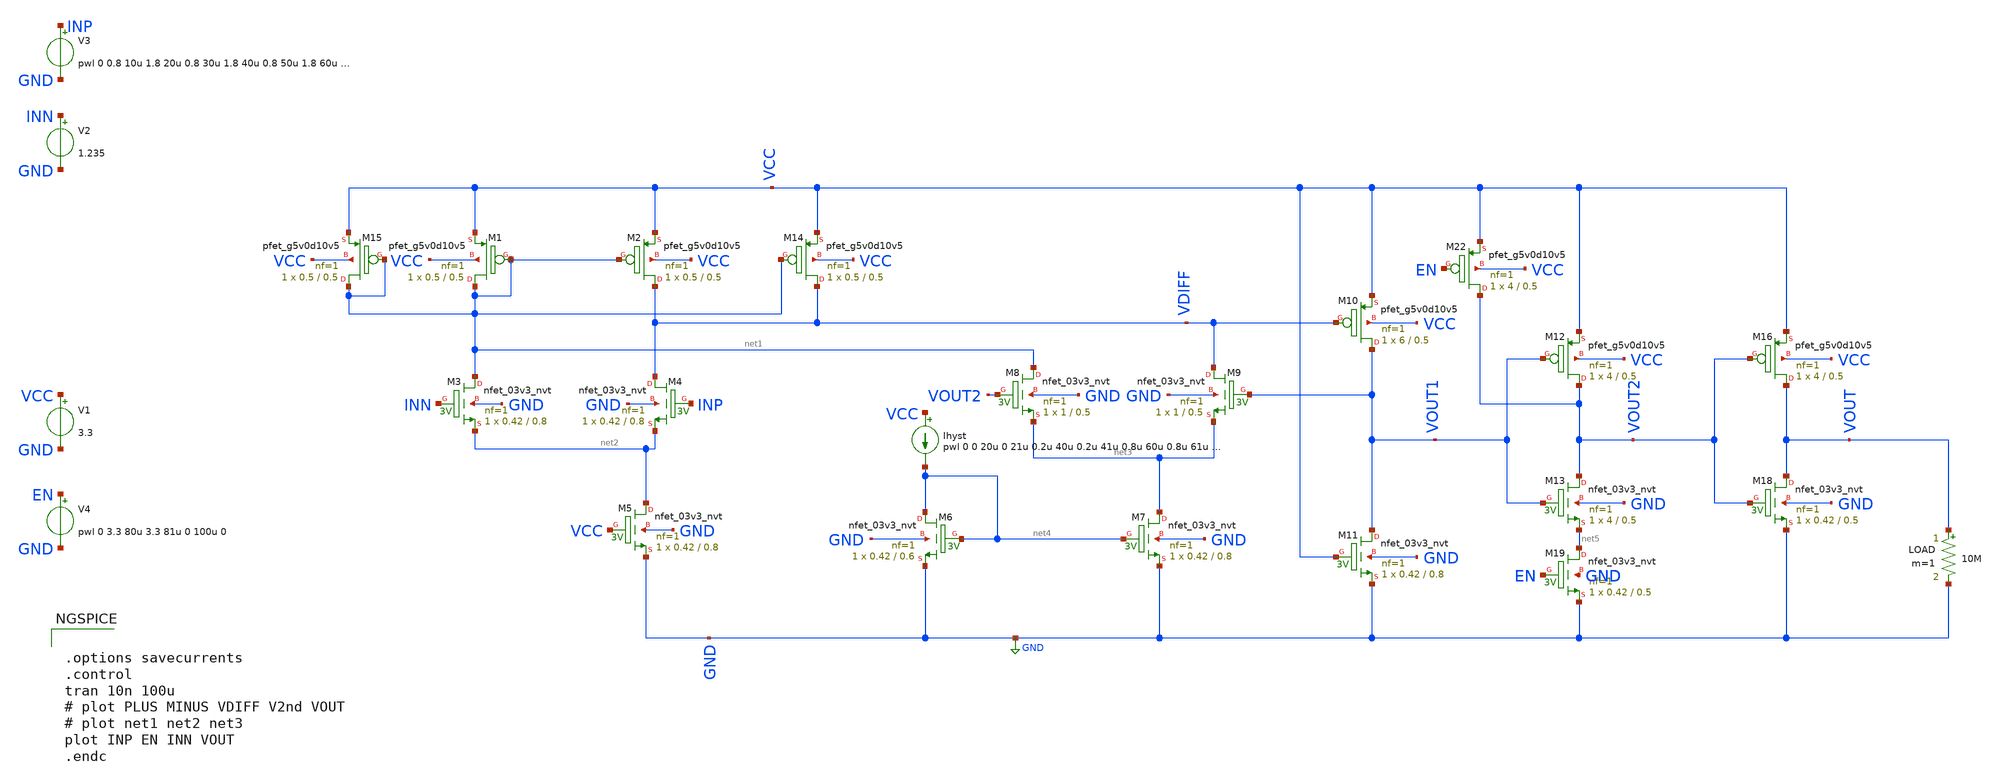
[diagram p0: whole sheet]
** sch_path: PreLayout/archive/comparator.sch
* Copyright 2020 Stefan Frederik Schippers
* Licensed under the Apache License, Version 2.0 (the "License");
* you may not use this file except in compliance with the License.
* You may obtain a copy of the License at
* https://www.apache.org/licenses/LICENSE-2.0
* Unless required by applicable law or agreed to in writing, software
* distributed under the License is distributed on an "AS IS" BASIS,
* WITHOUT WARRANTIES OR CONDITIONS OF ANY KIND, either express or implied.
* See the License for the specific language governing permissions and
* limitations under the License.
**.subckt comparator
Ihyst VCC net4 pwl 0 0 20u 0 21u 0.2u 40u 0.2u 41u 0.8u 60u 0.8u 61u 10u 100u 10u
V1 VCC GND 3.3
V2 INN GND 1.235
V3 INP GND pwl 0 0.8 10u 1.8 20u 0.8 30u 1.8 40u 0.8 50u 1.8 60u 0.8 70u 1.8 80u 0.8 90u 1.8 100u
+ 0.8
XM3 net1 INN net2 GND sky130_fd_pr__nfet_03v3_nvt L=0.8 W=0.42 nf=1 ad='int((nf+1)/2) * W/nf * 0.29'
+ as='int((nf+2)/2) * W/nf * 0.29' pd='2*int((nf+1)/2) * (W/nf + 0.29)' ps='2*int((nf+2)/2) * (W/nf + 0.29)'
+ nrd='0.29 / W' nrs='0.29 / W' sa=0 sb=0 sd=0 mult=1 m=1
XM4 VDIFF INP net2 GND sky130_fd_pr__nfet_03v3_nvt L=0.8 W=0.42 nf=1 ad='int((nf+1)/2) * W/nf * 0.29'
+ as='int((nf+2)/2) * W/nf * 0.29' pd='2*int((nf+1)/2) * (W/nf + 0.29)' ps='2*int((nf+2)/2) * (W/nf + 0.29)'
+ nrd='0.29 / W' nrs='0.29 / W' sa=0 sb=0 sd=0 mult=1 m=1
XM8 net1 VOUT2 net3 GND sky130_fd_pr__nfet_03v3_nvt L=0.5 W=1 nf=1 ad='int((nf+1)/2) * W/nf * 0.29' as='int((nf+2)/2) * W/nf * 0.29'
+ pd='2*int((nf+1)/2) * (W/nf + 0.29)' ps='2*int((nf+2)/2) * (W/nf + 0.29)' nrd='0.29 / W' nrs='0.29 / W'
+ sa=0 sb=0 sd=0 mult=1 m=1
XM9 VDIFF VOUT1 net3 GND sky130_fd_pr__nfet_03v3_nvt L=0.5 W=1 nf=1 ad='int((nf+1)/2) * W/nf * 0.29'
+ as='int((nf+2)/2) * W/nf * 0.29' pd='2*int((nf+1)/2) * (W/nf + 0.29)' ps='2*int((nf+2)/2) * (W/nf + 0.29)'
+ nrd='0.29 / W' nrs='0.29 / W' sa=0 sb=0 sd=0 mult=1 m=1
XM5 net2 VCC GND GND sky130_fd_pr__nfet_03v3_nvt L=0.8 W=0.42 nf=1 ad='int((nf+1)/2) * W/nf * 0.29' as='int((nf+2)/2) * W/nf * 0.29'
+ pd='2*int((nf+1)/2) * (W/nf + 0.29)' ps='2*int((nf+2)/2) * (W/nf + 0.29)' nrd='0.29 / W' nrs='0.29 / W'
+ sa=0 sb=0 sd=0 mult=1 m=1
XM2 VDIFF net1 VCC VCC sky130_fd_pr__pfet_g5v0d10v5 L=0.5 W=0.5 nf=1 ad='int((nf+1)/2) * W/nf * 0.29'
+ as='int((nf+2)/2) * W/nf * 0.29' pd='2*int((nf+1)/2) * (W/nf + 0.29)' ps='2*int((nf+2)/2) * (W/nf + 0.29)'
+ nrd='0.29 / W' nrs='0.29 / W' sa=0 sb=0 sd=0 mult=1 m=1
XM1 net1 net1 VCC VCC sky130_fd_pr__pfet_g5v0d10v5 L=0.5 W=0.5 nf=1 ad='int((nf+1)/2) * W/nf * 0.29'
+ as='int((nf+2)/2) * W/nf * 0.29' pd='2*int((nf+1)/2) * (W/nf + 0.29)' ps='2*int((nf+2)/2) * (W/nf + 0.29)'
+ nrd='0.29 / W' nrs='0.29 / W' sa=0 sb=0 sd=0 mult=1 m=1
XM12 VOUT2 VOUT1 VCC VCC sky130_fd_pr__pfet_g5v0d10v5 L=0.5 W=4 nf=1 ad='int((nf+1)/2) * W/nf * 0.29'
+ as='int((nf+2)/2) * W/nf * 0.29' pd='2*int((nf+1)/2) * (W/nf + 0.29)' ps='2*int((nf+2)/2) * (W/nf + 0.29)'
+ nrd='0.29 / W' nrs='0.29 / W' sa=0 sb=0 sd=0 mult=1 m=1
XM10 VOUT1 VDIFF VCC VCC sky130_fd_pr__pfet_g5v0d10v5 L=0.5 W=6 nf=1 ad='int((nf+1)/2) * W/nf * 0.29'
+ as='int((nf+2)/2) * W/nf * 0.29' pd='2*int((nf+1)/2) * (W/nf + 0.29)' ps='2*int((nf+2)/2) * (W/nf + 0.29)'
+ nrd='0.29 / W' nrs='0.29 / W' sa=0 sb=0 sd=0 mult=1 m=1
XM13 VOUT2 VOUT1 net5 GND sky130_fd_pr__nfet_03v3_nvt L=0.5 W=4 nf=1 ad='int((nf+1)/2) * W/nf * 0.29'
+ as='int((nf+2)/2) * W/nf * 0.29' pd='2*int((nf+1)/2) * (W/nf + 0.29)' ps='2*int((nf+2)/2) * (W/nf + 0.29)'
+ nrd='0.29 / W' nrs='0.29 / W' sa=0 sb=0 sd=0 mult=1 m=1
XM11 VOUT1 VCC GND GND sky130_fd_pr__nfet_03v3_nvt L=0.8 W=0.42 nf=1 ad='int((nf+1)/2) * W/nf * 0.29'
+ as='int((nf+2)/2) * W/nf * 0.29' pd='2*int((nf+1)/2) * (W/nf + 0.29)' ps='2*int((nf+2)/2) * (W/nf + 0.29)'
+ nrd='0.29 / W' nrs='0.29 / W' sa=0 sb=0 sd=0 mult=1 m=1
XM7 net3 net4 GND GND sky130_fd_pr__nfet_03v3_nvt L=0.8 W=0.42 nf=1 ad='int((nf+1)/2) * W/nf * 0.29'
+ as='int((nf+2)/2) * W/nf * 0.29' pd='2*int((nf+1)/2) * (W/nf + 0.29)' ps='2*int((nf+2)/2) * (W/nf + 0.29)'
+ nrd='0.29 / W' nrs='0.29 / W' sa=0 sb=0 sd=0 mult=1 m=1
XM6 net4 net4 GND GND sky130_fd_pr__nfet_03v3_nvt L=0.6 W=0.42 nf=1 ad='int((nf+1)/2) * W/nf * 0.29'
+ as='int((nf+2)/2) * W/nf * 0.29' pd='2*int((nf+1)/2) * (W/nf + 0.29)' ps='2*int((nf+2)/2) * (W/nf + 0.29)'
+ nrd='0.29 / W' nrs='0.29 / W' sa=0 sb=0 sd=0 mult=1 m=1
V4 EN GND pwl 0 3.3 80u 3.3 81u 0 100u 0
LOAD VOUT GND 10M m=1
XM14 VDIFF net1 VCC VCC sky130_fd_pr__pfet_g5v0d10v5 L=0.5 W=0.5 nf=1 ad='int((nf+1)/2) * W/nf * 0.29'
+ as='int((nf+2)/2) * W/nf * 0.29' pd='2*int((nf+1)/2) * (W/nf + 0.29)' ps='2*int((nf+2)/2) * (W/nf + 0.29)'
+ nrd='0.29 / W' nrs='0.29 / W' sa=0 sb=0 sd=0 mult=1 m=1
XM15 net1 net1 VCC VCC sky130_fd_pr__pfet_g5v0d10v5 L=0.5 W=0.5 nf=1 ad='int((nf+1)/2) * W/nf * 0.29'
+ as='int((nf+2)/2) * W/nf * 0.29' pd='2*int((nf+1)/2) * (W/nf + 0.29)' ps='2*int((nf+2)/2) * (W/nf + 0.29)'
+ nrd='0.29 / W' nrs='0.29 / W' sa=0 sb=0 sd=0 mult=1 m=1
XM16 VOUT VOUT2 VCC VCC sky130_fd_pr__pfet_g5v0d10v5 L=0.5 W=4 nf=1 ad='int((nf+1)/2) * W/nf * 0.29'
+ as='int((nf+2)/2) * W/nf * 0.29' pd='2*int((nf+1)/2) * (W/nf + 0.29)' ps='2*int((nf+2)/2) * (W/nf + 0.29)'
+ nrd='0.29 / W' nrs='0.29 / W' sa=0 sb=0 sd=0 mult=1 m=1
XM18 VOUT VOUT2 GND GND sky130_fd_pr__nfet_03v3_nvt L=0.5 W=0.42 nf=1 ad='int((nf+1)/2) * W/nf * 0.29'
+ as='int((nf+2)/2) * W/nf * 0.29' pd='2*int((nf+1)/2) * (W/nf + 0.29)' ps='2*int((nf+2)/2) * (W/nf + 0.29)'
+ nrd='0.29 / W' nrs='0.29 / W' sa=0 sb=0 sd=0 mult=1 m=1
XM19 net5 EN GND GND sky130_fd_pr__nfet_03v3_nvt L=0.5 W=0.42 nf=1 ad='int((nf+1)/2) * W/nf * 0.29' as='int((nf+2)/2) * W/nf * 0.29'
+ pd='2*int((nf+1)/2) * (W/nf + 0.29)' ps='2*int((nf+2)/2) * (W/nf + 0.29)' nrd='0.29 / W' nrs='0.29 / W'
+ sa=0 sb=0 sd=0 mult=1 m=1
XM22 VOUT2 EN VCC VCC sky130_fd_pr__pfet_g5v0d10v5 L=0.5 W=4 nf=1 ad='int((nf+1)/2) * W/nf * 0.29' as='int((nf+2)/2) * W/nf * 0.29'
+ pd='2*int((nf+1)/2) * (W/nf + 0.29)' ps='2*int((nf+2)/2) * (W/nf + 0.29)' nrd='0.29 / W' nrs='0.29 / W'
+ sa=0 sb=0 sd=0 mult=1 m=1
**** begin user architecture code

.include $::SKYWATER_MODELS/cells/nfet_01v8/sky130_fd_pr__nfet_01v8__tt.corner.spice
.include $::SKYWATER_MODELS/cells/nfet_01v8_lvt/sky130_fd_pr__nfet_01v8_lvt__tt.corner.spice
.include $::SKYWATER_MODELS/cells/pfet_01v8/sky130_fd_pr__pfet_01v8__tt.corner.spice
.include $::SKYWATER_MODELS/cells/nfet_03v3_nvt/sky130_fd_pr__nfet_03v3_nvt__tt.corner.spice
.include $::SKYWATER_MODELS/cells/nfet_05v0_nvt/sky130_fd_pr__nfet_05v0_nvt__tt.corner.spice
.include $::SKYWATER_MODELS/cells/esd_nfet_01v8/sky130_fd_pr__esd_nfet_01v8__tt.corner.spice
.include $::SKYWATER_MODELS/cells/pfet_01v8_lvt/sky130_fd_pr__pfet_01v8_lvt__tt.corner.spice
.include $::SKYWATER_MODELS/cells/pfet_01v8_hvt/sky130_fd_pr__pfet_01v8_hvt__tt.corner.spice
.include $::SKYWATER_MODELS/cells/esd_pfet_g5v0d10v5/sky130_fd_pr__esd_pfet_g5v0d10v5__tt.corner.spice
.include $::SKYWATER_MODELS/cells/pfet_g5v0d10v5/sky130_fd_pr__pfet_g5v0d10v5__tt.corner.spice
.include $::SKYWATER_MODELS/cells/pfet_g5v0d16v0/sky130_fd_pr__pfet_g5v0d16v0__tt.corner.spice
.include $::SKYWATER_MODELS/cells/nfet_g5v0d10v5/sky130_fd_pr__nfet_g5v0d10v5__tt.corner.spice
.include $::SKYWATER_MODELS/cells/nfet_g5v0d16v0/sky130_fd_pr__nfet_g5v0d16v0__tt_discrete.corner.spice
.include $::SKYWATER_MODELS/cells/esd_nfet_g5v0d10v5/sky130_fd_pr__esd_nfet_g5v0d10v5__tt.corner.spice
.include $::SKYWATER_MODELS/models/corners/tt/nonfet.spice
* Mismatch parameters
.include $::SKYWATER_MODELS/cells/nfet_01v8/sky130_fd_pr__nfet_01v8__mismatch.corner.spice
.include $::SKYWATER_MODELS/cells/pfet_01v8/sky130_fd_pr__pfet_01v8__mismatch.corner.spice
.include $::SKYWATER_MODELS/cells/nfet_01v8_lvt/sky130_fd_pr__nfet_01v8_lvt__mismatch.corner.spice
.include $::SKYWATER_MODELS/cells/pfet_01v8_lvt/sky130_fd_pr__pfet_01v8_lvt__mismatch.corner.spice
.include $::SKYWATER_MODELS/cells/pfet_01v8_hvt/sky130_fd_pr__pfet_01v8_hvt__mismatch.corner.spice
.include $::SKYWATER_MODELS/cells/nfet_g5v0d10v5/sky130_fd_pr__nfet_g5v0d10v5__mismatch.corner.spice
.include $::SKYWATER_MODELS/cells/pfet_g5v0d10v5/sky130_fd_pr__pfet_g5v0d10v5__mismatch.corner.spice
.include $::SKYWATER_MODELS/cells/nfet_05v0_nvt/sky130_fd_pr__nfet_05v0_nvt__mismatch.corner.spice
.include $::SKYWATER_MODELS/cells/nfet_03v3_nvt/sky130_fd_pr__nfet_03v3_nvt__mismatch.corner.spice
* Resistor$::SKYWATER_MODELS/Capacitor
.include $::SKYWATER_MODELS/models/r+c/res_typical__cap_typical.spice
.include $::SKYWATER_MODELS/models/r+c/res_typical__cap_typical__lin.spice
* Special cells
.include $::SKYWATER_MODELS/models/corners/tt/specialized_cells.spice
* All models
.include $::SKYWATER_MODELS/models/all.spice
* Corner
.include $::SKYWATER_MODELS/models/corners/tt/rf.spice



.options savecurrents
.control
tran 10n 100u
# plot PLUS MINUS VDIFF V2nd VOUT
# plot net1 net2 net3
plot INP EN INN VOUT
.endc


**** end user architecture code
**.ends
.GLOBAL GND
.end
